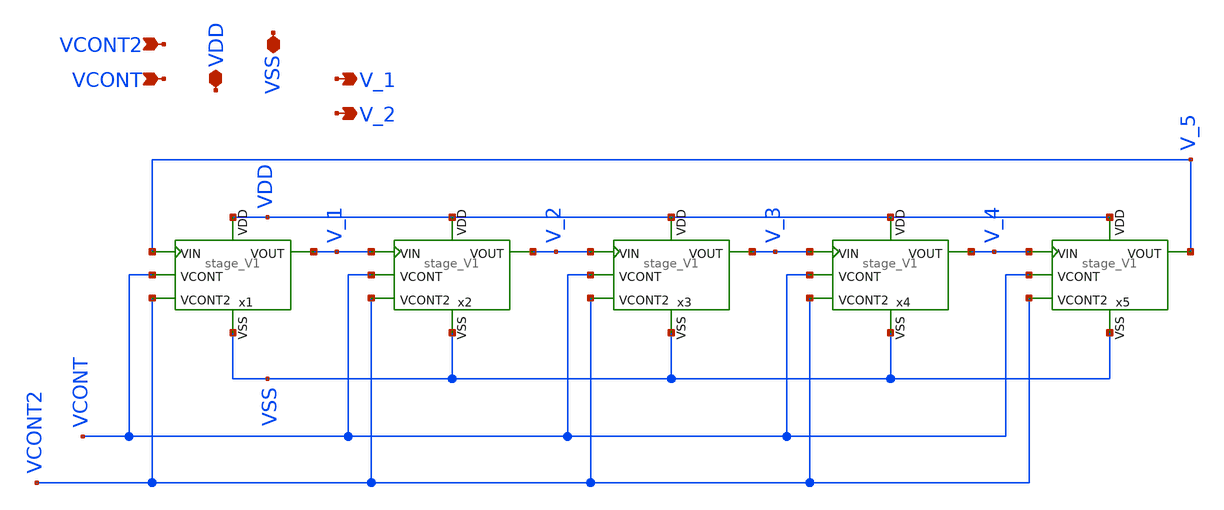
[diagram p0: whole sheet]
** sch_path: xschem/VCO/VCO_V1.sch
**.subckt VCO_V1 VCONT VDD VSS V_1 V_2 VCONT2
*.ipin VCONT
*.iopin VDD
*.iopin VSS
*.opin V_1
*.opin V_2
*.ipin VCONT2
x1 VDD VCONT V_1 V_5 VSS VCONT2 stage_V1
x2 VDD VCONT V_2 V_1 VSS VCONT2 stage_V1
x3 VDD VCONT V_3 V_2 VSS VCONT2 stage_V1
x4 VDD VCONT V_4 V_3 VSS VCONT2 stage_V1
x5 VDD VCONT V_5 V_4 VSS VCONT2 stage_V1
**.ends

* expanding   symbol:  ../VCO/stage_V1.sym # of pins=6
** sym_path: xschem/VCO/stage_V1.sym
** sch_path: xschem/VCO/stage_V1.sch
.subckt stage_V1 VDD VCONT VOUT VIN VSS VCONT2
*.ipin VCONT2
*.ipin VIN
*.opin VOUT
*.iopin VDD
*.iopin VSS
*.ipin VCONT
XMN1 VSS net2 net2 VSS sg13_hv_nmos w={w_MN1} l={l_MN1} ng=1 m={m_MN1} mm_ok=1
XMN2 VSS net2 net3 VSS sg13_hv_nmos w={w_MN2} l={l_MN2} ng=1 m={m_MN2} mm_ok=1
XMN3 VSS net2 VdsMN3 VSS sg13_hv_nmos w={w_MN3} l={l_MN3} ng=1 m={m_MN3} mm_ok=1
XMP1a VCN VCONT VDD VDD sg13_hv_pmos w={w_MP1a} l={l_MP1a} ng=1 m={m_MP1a} mm_ok=1
XMP2 VCP VCP VDD VDD sg13_hv_pmos w={w_MP2} l={l_MP2} ng=1 m={m_MP2} mm_ok=1
XMP3 net4 VCP VDD VDD sg13_hv_pmos w={w_MP3} l={l_MP3} ng=1 m={m_MP3} mm_ok=1
XMP7 net1 VIN VSMP4 VDD sg13_hv_pmos w={w_MP4} l={l_MP4} ng=1 m={m_MP4} mm_ok=1
XMN4 VdsMN3 VIN net1 VSS sg13_hv_nmos w={w_MN4} l={l_MN4} ng=1 m={m_MN4} mm_ok=1
XMP1b VCN VCONT2 VDD VDD sg13_hv_pmos w={w_MP1b} l={l_MP1b} ng=1 m={m_MP1b} mm_ok=1
VIcont1 VCN net2 0
.save i(vicont1)
VIcont2 VCP net3 0
.save i(vicont2)
VIcont3 net4 VSMP4 0
.save i(vicont3)
VIcont4 net1 VOUT 0
.save i(vicont4)
.ends

.end
